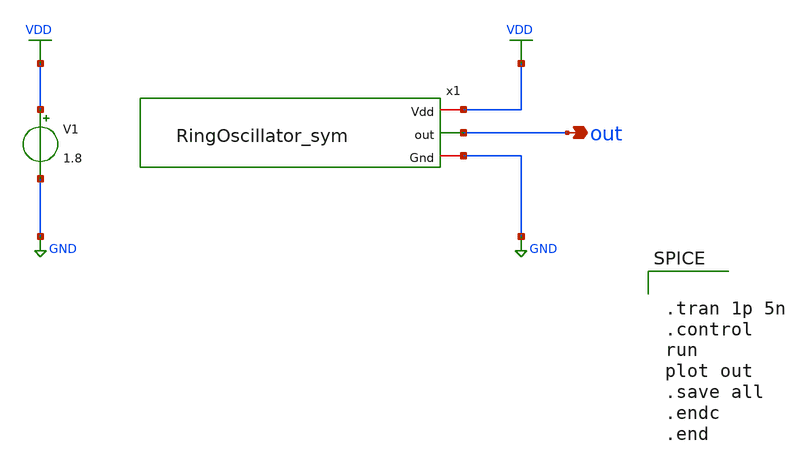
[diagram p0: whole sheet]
** sch_path: Week_3/RingOscillator_PreLayout/RingOscillator_tb.sch
**.subckt RingOscillator_tb out
*.opin out
x1 VDD out GND RingOscillator_sym
V1 VDD GND 1.8
**** begin user architecture code


.lib /home/swagatika/open_pdks/sky130/sky130A/libs.tech/ngspice/sky130.lib.spice tt

.save all





.tran 1p 5n
.control
run
plot out
.save all
.endc
.end


**** end user architecture code
**.ends
.GLOBAL GND
.GLOBAL VDD
.end
